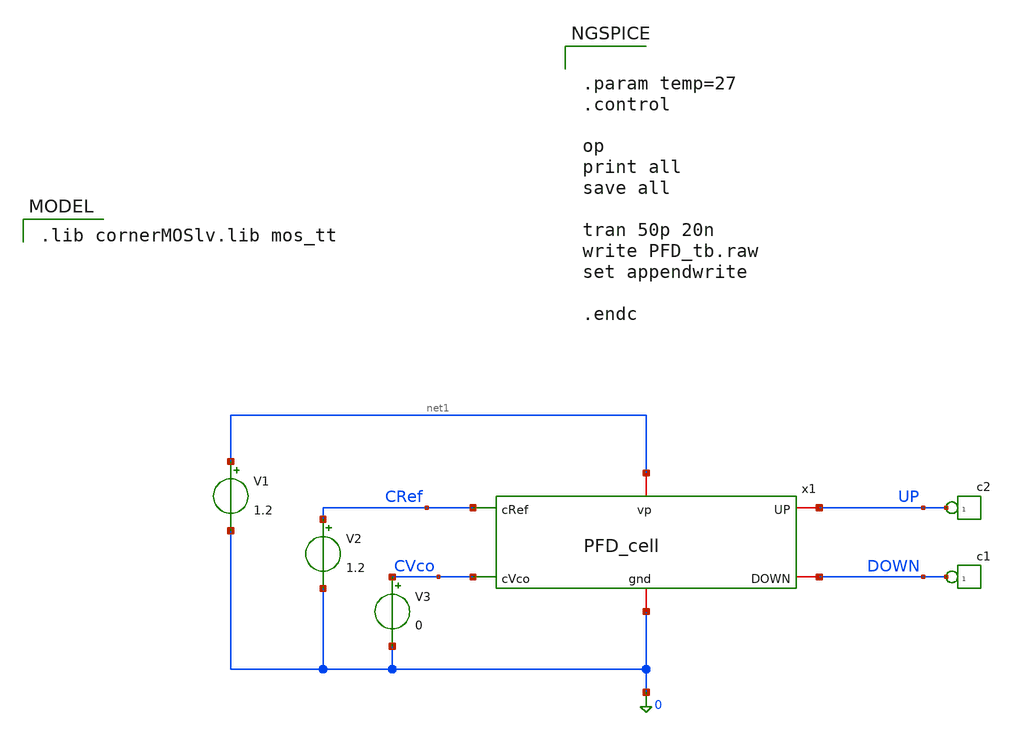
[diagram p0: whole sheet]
** sch_path: PFD/PFD_tb.sch
**.subckt PFD_tb
x1 0 net1 CRef UP DOWN CVco PFD_cell
V1 net1 0 1.2
V2 CRef 0 1.2
V3 CVco 0 0
*connector(1,1) ?1 DOWN
*connector(1,1) ?1 UP
**** begin user architecture code
 .lib cornerMOSlv.lib mos_tt



.param temp=27
.control

op
print all
save all

tran 50p 20n
write PFD_tb.raw
set appendwrite

.endc


**** end user architecture code
**.ends
.end
